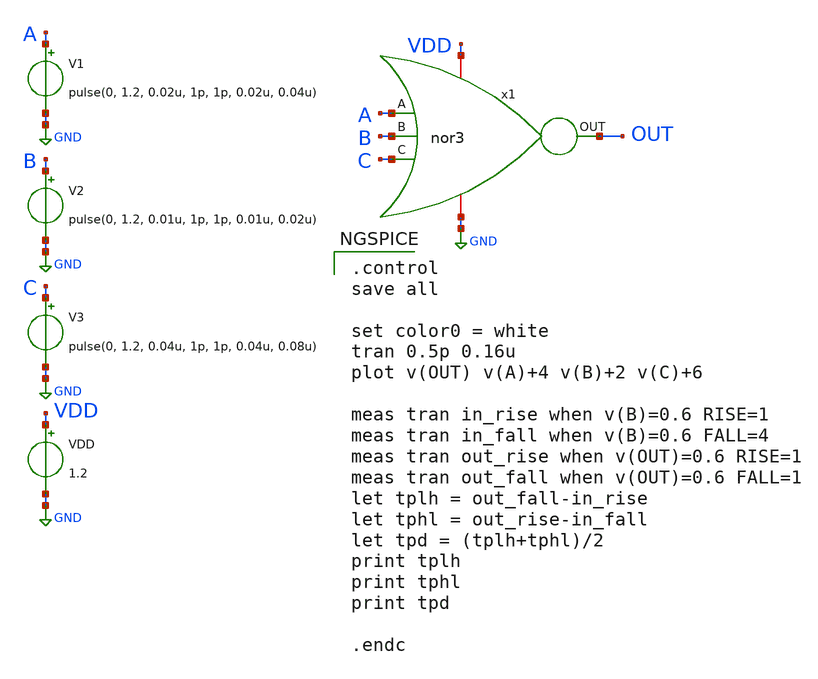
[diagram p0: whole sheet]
** sch_path: design/NOR3/xschem/nor3_tb.sch
**.subckt nor3_tb
V1 A GND pulse(0, 1.2, 0.02u, 1p, 1p, 0.02u, 0.04u)
V2 B GND pulse(0, 1.2, 0.01u, 1p, 1p, 0.01u, 0.02u)
VDD VDD GND 1.2
x1 VDD A B C OUT GND nor3
V3 C GND pulse(0, 1.2, 0.04u, 1p, 1p, 0.04u, 0.08u)
**** begin user architecture code

** opencircuitdesign pdks install
.lib $::SKYWATER_MODELS/sky130.lib.spice tt_mm



.control
save all

set color0 = white
tran 0.5p 0.16u
plot v(OUT) v(A)+4 v(B)+2 v(C)+6

meas tran in_rise when v(B)=0.6 RISE=1
meas tran in_fall when v(B)=0.6 FALL=4
meas tran out_rise when v(OUT)=0.6 RISE=1
meas tran out_fall when v(OUT)=0.6 FALL=1
let tplh = out_fall-in_rise
let tphl = out_rise-in_fall
let tpd = (tplh+tphl)/2
print tplh
print tphl
print tpd

.endc

**** end user architecture code
**.ends
.GLOBAL GND
.end
